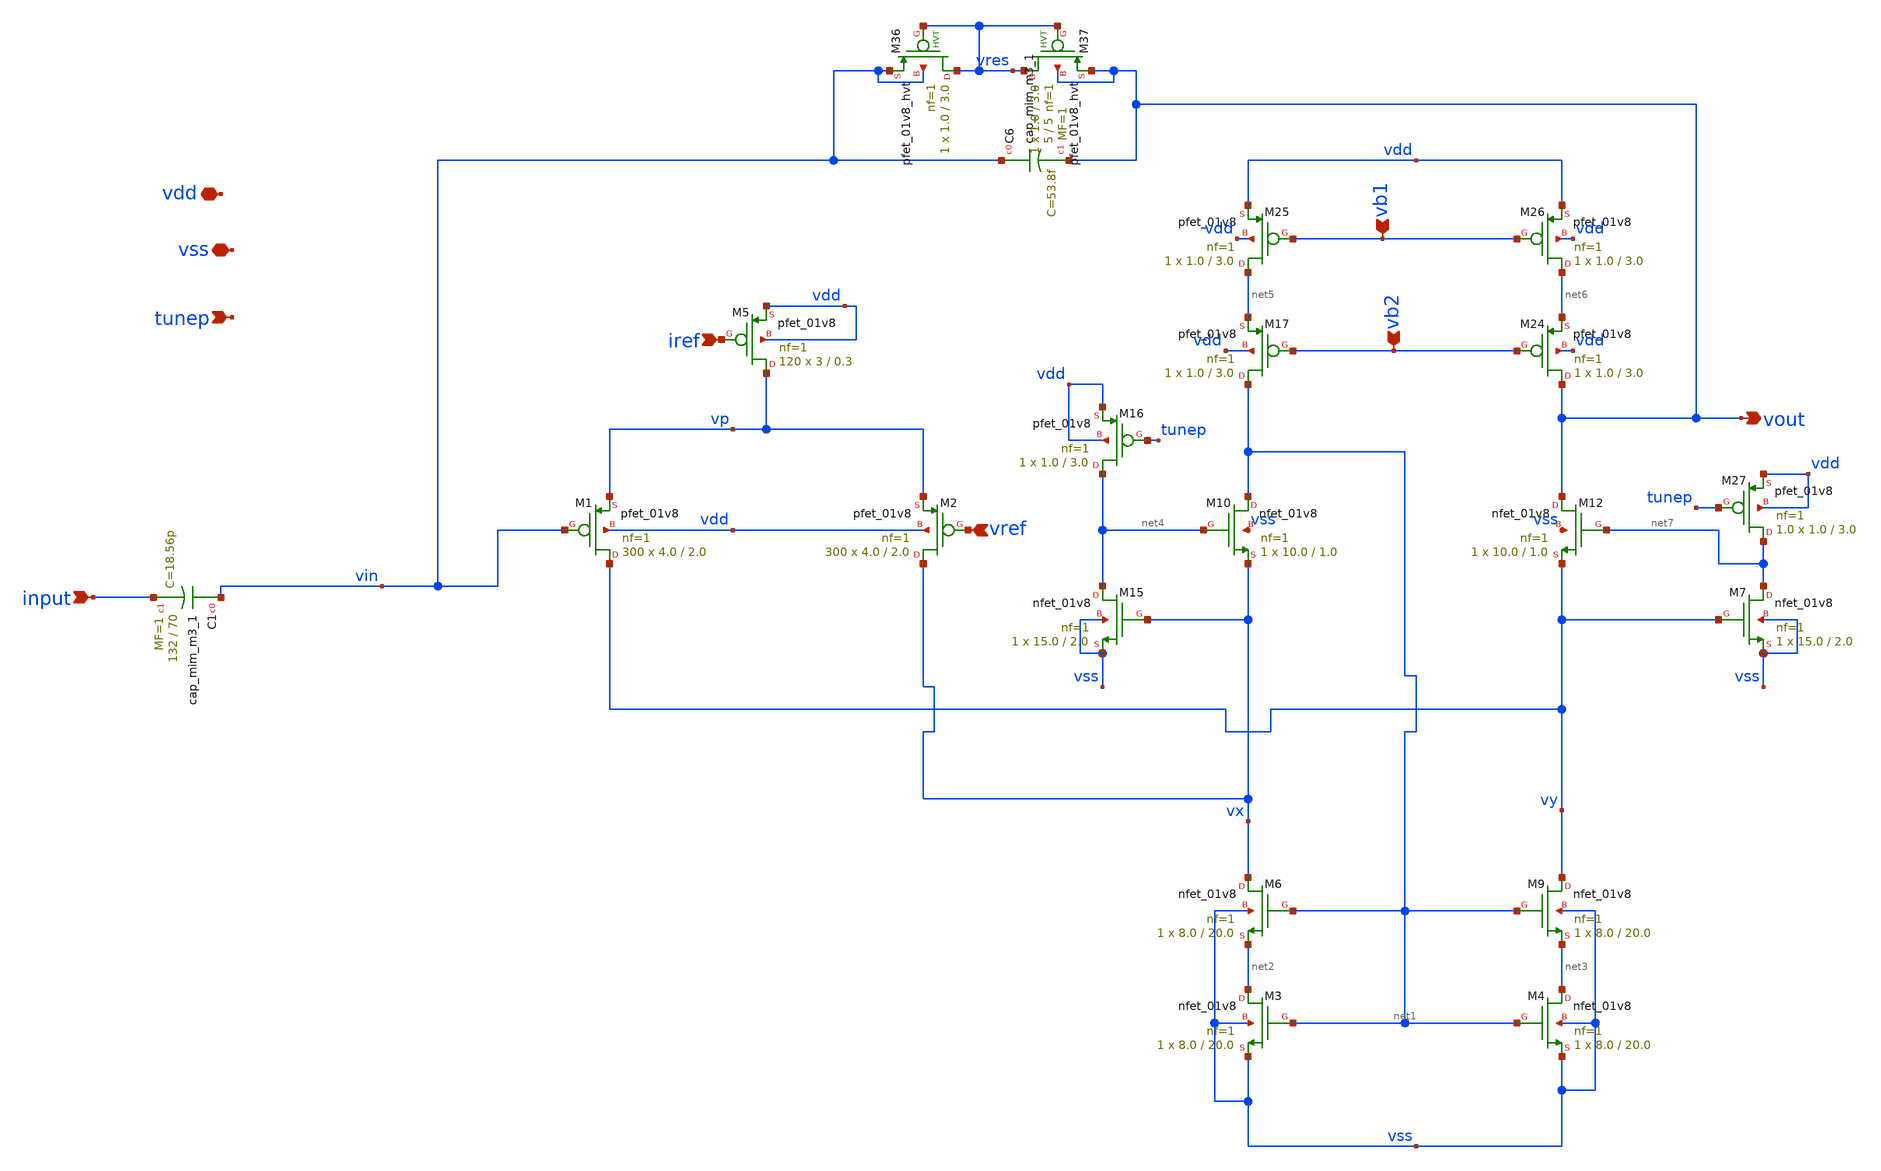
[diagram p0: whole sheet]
** sch_path: design/xschem/low_noise_amp_fc_v3.sch
**.subckt low_noise_amp_fc_v3 vdd vss vref iref input vout tunep vb1 vb2
*.iopin vdd
*.iopin vss
*.ipin vref
*.ipin iref
*.ipin input
*.opin vout
*.ipin tunep
*.ipin vb1
*.ipin vb2
XM1 vy vin vp vdd sky130_fd_pr__pfet_01v8 L=2.0 W=4.0 nf=1 ad='W * 0.29' as='W * 0.29' pd='2 * (W + 0.29)'
+ ps='2 * (W + 0.29)' nrd='0.29 / W' nrs='0.29 / W' sa=0 sb=0 sd=0 mult=300 m=300
XM2 vx vref vp vdd sky130_fd_pr__pfet_01v8 L=2.0 W=4.0 nf=1 ad='W * 0.29' as='W * 0.29' pd='2 * (W + 0.29)'
+ ps='2 * (W + 0.29)' nrd='0.29 / W' nrs='0.29 / W' sa=0 sb=0 sd=0 mult=300 m=300
XM5 vp iref vdd vdd sky130_fd_pr__pfet_01v8 L=0.3 W=3 nf=1 ad='W * 0.29' as='W * 0.29' pd='2 * (W + 0.29)'
+ ps='2 * (W + 0.29)' nrd='0.29 / W' nrs='0.29 / W' sa=0 sb=0 sd=0 mult=120 m=120
XC6 vin vout sky130_fd_pr__cap_mim_m3_1 W=5 L=5 MF=1 m=1
XM6 vx net1 net2 vss sky130_fd_pr__nfet_01v8 L=20.0 W=8.0 nf=1 ad='W * 0.29' as='W * 0.29' pd='2 * (W + 0.29)'
+ ps='2 * (W + 0.29)' nrd='0.29 / W' nrs='0.29 / W' sa=0 sb=0 sd=0 mult=1 m=1
XM9 vy net1 net3 vss sky130_fd_pr__nfet_01v8 L=20.0 W=8.0 nf=1 ad='W * 0.29' as='W * 0.29' pd='2 * (W + 0.29)'
+ ps='2 * (W + 0.29)' nrd='0.29 / W' nrs='0.29 / W' sa=0 sb=0 sd=0 mult=1 m=1
XM10 net1 net4 vx vss sky130_fd_pr__nfet_01v8 L=1.0 W=10.0 nf=1 ad='W * 0.29' as='W * 0.29' pd='2 * (W + 0.29)'
+ ps='2 * (W + 0.29)' nrd='0.29 / W' nrs='0.29 / W' sa=0 sb=0 sd=0 mult=1 m=1
XM12 vout net7 vy vss sky130_fd_pr__nfet_01v8 L=1.0 W=10.0 nf=1 ad='W * 0.29' as='W * 0.29' pd='2 * (W + 0.29)'
+ ps='2 * (W + 0.29)' nrd='0.29 / W' nrs='0.29 / W' sa=0 sb=0 sd=0 mult=1 m=1
XM15 net4 vx vss vss sky130_fd_pr__nfet_01v8 L=2.0 W=15.0 nf=1 ad='W * 0.29' as='W * 0.29' pd='2 * (W + 0.29)'
+ ps='2 * (W + 0.29)' nrd='0.29 / W' nrs='0.29 / W' sa=0 sb=0 sd=0 mult=1 m=1
XM16 net4 tunep vdd vdd sky130_fd_pr__pfet_01v8 L=3.0 W=1.0 nf=1 ad='W * 0.29' as='W * 0.29' pd='2 * (W + 0.29)'
+ ps='2 * (W + 0.29)' nrd='0.29 / W' nrs='0.29 / W' sa=0 sb=0 sd=0 mult=1 m=1
XM17 net1 vb2 net5 vdd sky130_fd_pr__pfet_01v8 L=3.0 W=1.0 nf=1 ad='W * 0.29' as='W * 0.29' pd='2 * (W + 0.29)'
+ ps='2 * (W + 0.29)' nrd='0.29 / W' nrs='0.29 / W' sa=0 sb=0 sd=0 mult=1 m=1
XM24 vout vb2 net6 vdd sky130_fd_pr__pfet_01v8 L=3.0 W=1.0 nf=1 ad='W * 0.29' as='W * 0.29' pd='2 * (W + 0.29)'
+ ps='2 * (W + 0.29)' nrd='0.29 / W' nrs='0.29 / W' sa=0 sb=0 sd=0 mult=1 m=1
XM25 net5 vb1 vdd vdd sky130_fd_pr__pfet_01v8 L=3.0 W=1.0 nf=1 ad='W * 0.29' as='W * 0.29' pd='2 * (W + 0.29)'
+ ps='2 * (W + 0.29)' nrd='0.29 / W' nrs='0.29 / W' sa=0 sb=0 sd=0 mult=1 m=1
XM26 net6 vb1 vdd vdd sky130_fd_pr__pfet_01v8 L=3.0 W=1.0 nf=1 ad='W * 0.29' as='W * 0.29' pd='2 * (W + 0.29)'
+ ps='2 * (W + 0.29)' nrd='0.29 / W' nrs='0.29 / W' sa=0 sb=0 sd=0 mult=1 m=1
XM7 net7 vy vss vss sky130_fd_pr__nfet_01v8 L=2.0 W=15.0 nf=1 ad='W * 0.29' as='W * 0.29' pd='2 * (W + 0.29)'
+ ps='2 * (W + 0.29)' nrd='0.29 / W' nrs='0.29 / W' sa=0 sb=0 sd=0 mult=1 m=1
XM27 net7 tunep vdd vdd sky130_fd_pr__pfet_01v8 L=3.0 W=1.0 nf=1 ad='W * 0.29' as='W * 0.29' pd='2 * (W + 0.29)'
+ ps='2 * (W + 0.29)' nrd='0.29 / W' nrs='0.29 / W' sa=0 sb=0 sd=0 mult=1.0 m=1.0
XM36 vres vres vin vin sky130_fd_pr__pfet_01v8_hvt L=3.0 W=1.0 nf=1 ad='int((nf+1)/2) * W/nf * 0.29'
+ as='int((nf+2)/2) * W/nf * 0.29' pd='2*int((nf+1)/2) * (W/nf + 0.29)' ps='2*int((nf+2)/2) * (W/nf + 0.29)'
+ nrd='0.29 / W' nrs='0.29 / W' sa=0 sb=0 sd=0 mult=1 m=1
XM37 vres vres vout vout sky130_fd_pr__pfet_01v8_hvt L=3.0 W=1.0 nf=1 ad='int((nf+1)/2) * W/nf * 0.29'
+ as='int((nf+2)/2) * W/nf * 0.29' pd='2*int((nf+1)/2) * (W/nf + 0.29)' ps='2*int((nf+2)/2) * (W/nf + 0.29)'
+ nrd='0.29 / W' nrs='0.29 / W' sa=0 sb=0 sd=0 mult=1 m=1
XM3 net2 net1 vss vss sky130_fd_pr__nfet_01v8 L=20.0 W=8.0 nf=1 ad='W * 0.29' as='W * 0.29' pd='2 * (W + 0.29)'
+ ps='2 * (W + 0.29)' nrd='0.29 / W' nrs='0.29 / W' sa=0 sb=0 sd=0 mult=1 m=1
XM4 net3 net1 vss vss sky130_fd_pr__nfet_01v8 L=20.0 W=8.0 nf=1 ad='W * 0.29' as='W * 0.29' pd='2 * (W + 0.29)'
+ ps='2 * (W + 0.29)' nrd='0.29 / W' nrs='0.29 / W' sa=0 sb=0 sd=0 mult=1 m=1
XC1 vin input sky130_fd_pr__cap_mim_m3_1 W=132 L=70 MF=1 m=1
**.ends
.end
